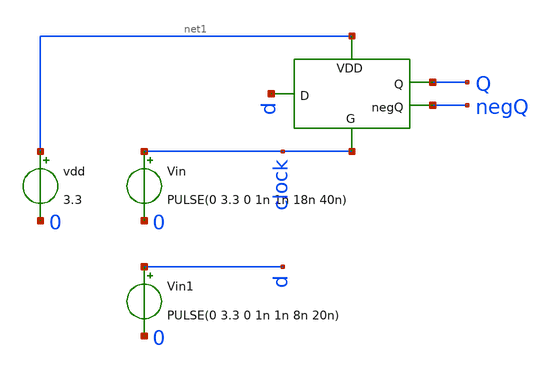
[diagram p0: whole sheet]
** sch_path: initial_notebooks_2023/accepted_notebooks/Current-Steering-DAC/DAC/Test_DLatch.sch
**.subckt Test_DLatch
Vin clock 0 PULSE(0 3.3 0 1n 1n 18n 40n)
vdd net1 0 3.3
x1 d clock net1 Q negQ DLatch
Vin1 d 0 PULSE(0 3.3 0 1n 1n 8n 20n)
**** begin user architecture code




.include /foss/pdks/gf180mcuC/libs.tech/ngspice/design.ngspice
.lib /foss/pdks/gf180mcuC/libs.tech/ngspice/sm141064.ngspice typical


.control
	tran 1n 150n
	plot v(clock) v(d)
	plot v(Q)
.endc
.save all




**** end user architecture code
**.ends
.end
